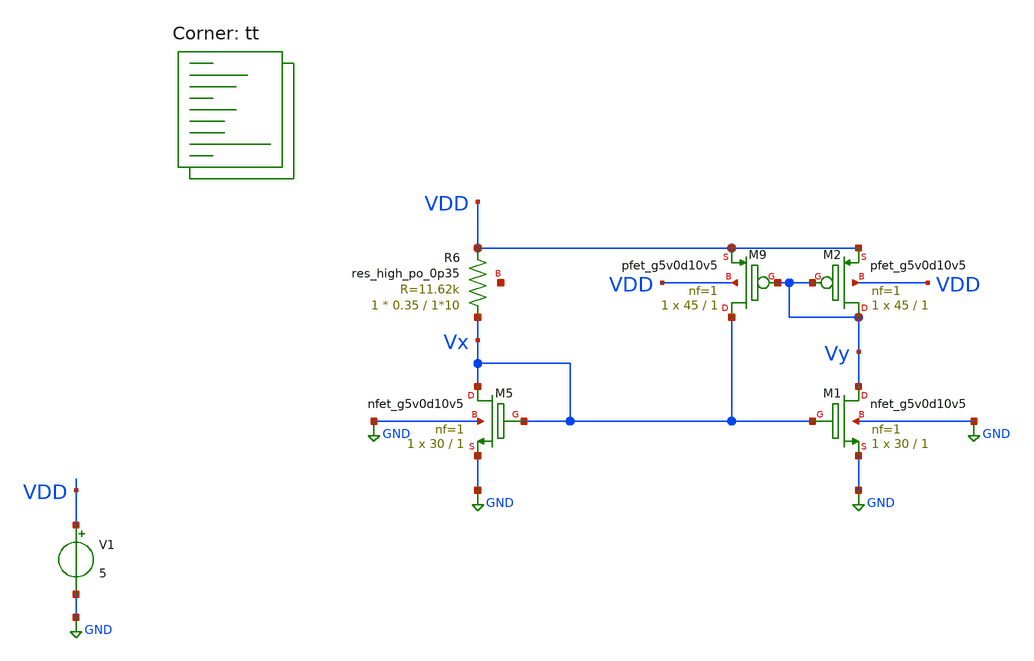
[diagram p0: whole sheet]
** sch_path: amplifiers/current_mirrors/exercises/6/current_mirror_test.sch
**.subckt current_mirror_test
V1 VDD GND 5
XM5 Vx Vx GND GND sky130_fd_pr__nfet_g5v0d10v5 L=1 W=30 nf=1 ad='int((1 + 1)/2) * 30 / 1 * 0.29' as='int((1 + 2)/2) * 30 / 1 * 0.29'
+ pd='2*int((1 + 1)/2) * (30 / 1 + 0.29)' ps='2*int((1 + 2)/2) * (30 / 1 + 0.29)' nrd='0.29 / 30 ' nrs='0.29 / 30 '
+ sa=0 sb=0 sd=0 mult=1 m=1
XR6 Vx VDD net1 sky130_fd_pr__res_high_po_0p35 L=1*10 mult=1 m=1
XM1 Vy Vx GND GND sky130_fd_pr__nfet_g5v0d10v5 L=1 W=30 nf=1 ad='int((1 + 1)/2) * 30 / 1 * 0.29' as='int((1 + 2)/2) * 30 / 1 * 0.29'
+ pd='2*int((1 + 1)/2) * (30 / 1 + 0.29)' ps='2*int((1 + 2)/2) * (30 / 1 + 0.29)' nrd='0.29 / 30 ' nrs='0.29 / 30 '
+ sa=0 sb=0 sd=0 mult=1 m=1
XM9 Vx Vy VDD VDD sky130_fd_pr__pfet_g5v0d10v5 L=1 W=45 nf=1 ad='int((1 + 1)/2) * 45 / 1 * 0.29' as='int((1 + 2)/2) * 45 / 1 * 0.29'
+ pd='2*int((1 + 1)/2) * (45 / 1 + 0.29)' ps='2*int((1 + 2)/2) * (45 / 1 + 0.29)' nrd='0.29 / 45 ' nrs='0.29 / 45 '
+ sa=0 sb=0 sd=0 mult=1 m=1
XM2 Vy Vy VDD VDD sky130_fd_pr__pfet_g5v0d10v5 L=1 W=45 nf=1 ad='int((1 + 1)/2) * 45 / 1 * 0.29' as='int((1 + 2)/2) * 45 / 1 * 0.29'
+ pd='2*int((1 + 1)/2) * (45 / 1 + 0.29)' ps='2*int((1 + 2)/2) * (45 / 1 + 0.29)' nrd='0.29 / 45 ' nrs='0.29 / 45 '
+ sa=0 sb=0 sd=0 mult=1 m=1
**** begin user architecture code

**************************************************************
**************************************************************
**************************************************************
**************************************************************
**************************************************************
*LIBs*********************************************************
**************************************************************
**************************************************************
**************************************************************
**************************************************************
**************************************************************
*.lib $::SKYWATER_MODELS/sky130.lib.spice tt
* chose the corners in the corner file
* tt_mm for mismatch
* ss ff sf fs standart corners
* ll hh lh hl capacitor and resistors corners
* mc for total process variation including corners
**************************************************************
**************************************************************
**************************************************************
**************************************************************
**************************************************************
*Corners/montecarlo options***********************************
**************************************************************
**************************************************************
**************************************************************
**************************************************************
**************************************************************
.TEMP 27
**************************************************************
**************************************************************
**************************************************************
**************************************************************
*SIMULATION and Plots*****************************************
**************************************************************
**************************************************************
**************************************************************
**************************************************************
.control
save all
dc V1 0 5 0.001
plot v(Vx) v(Vy)
plot deriv(v(Vy))

.endc

.lib $::SKYWATER_MODELS/sky130.lib.spice tt
**** end user architecture code
**.ends
.GLOBAL GND
.end
